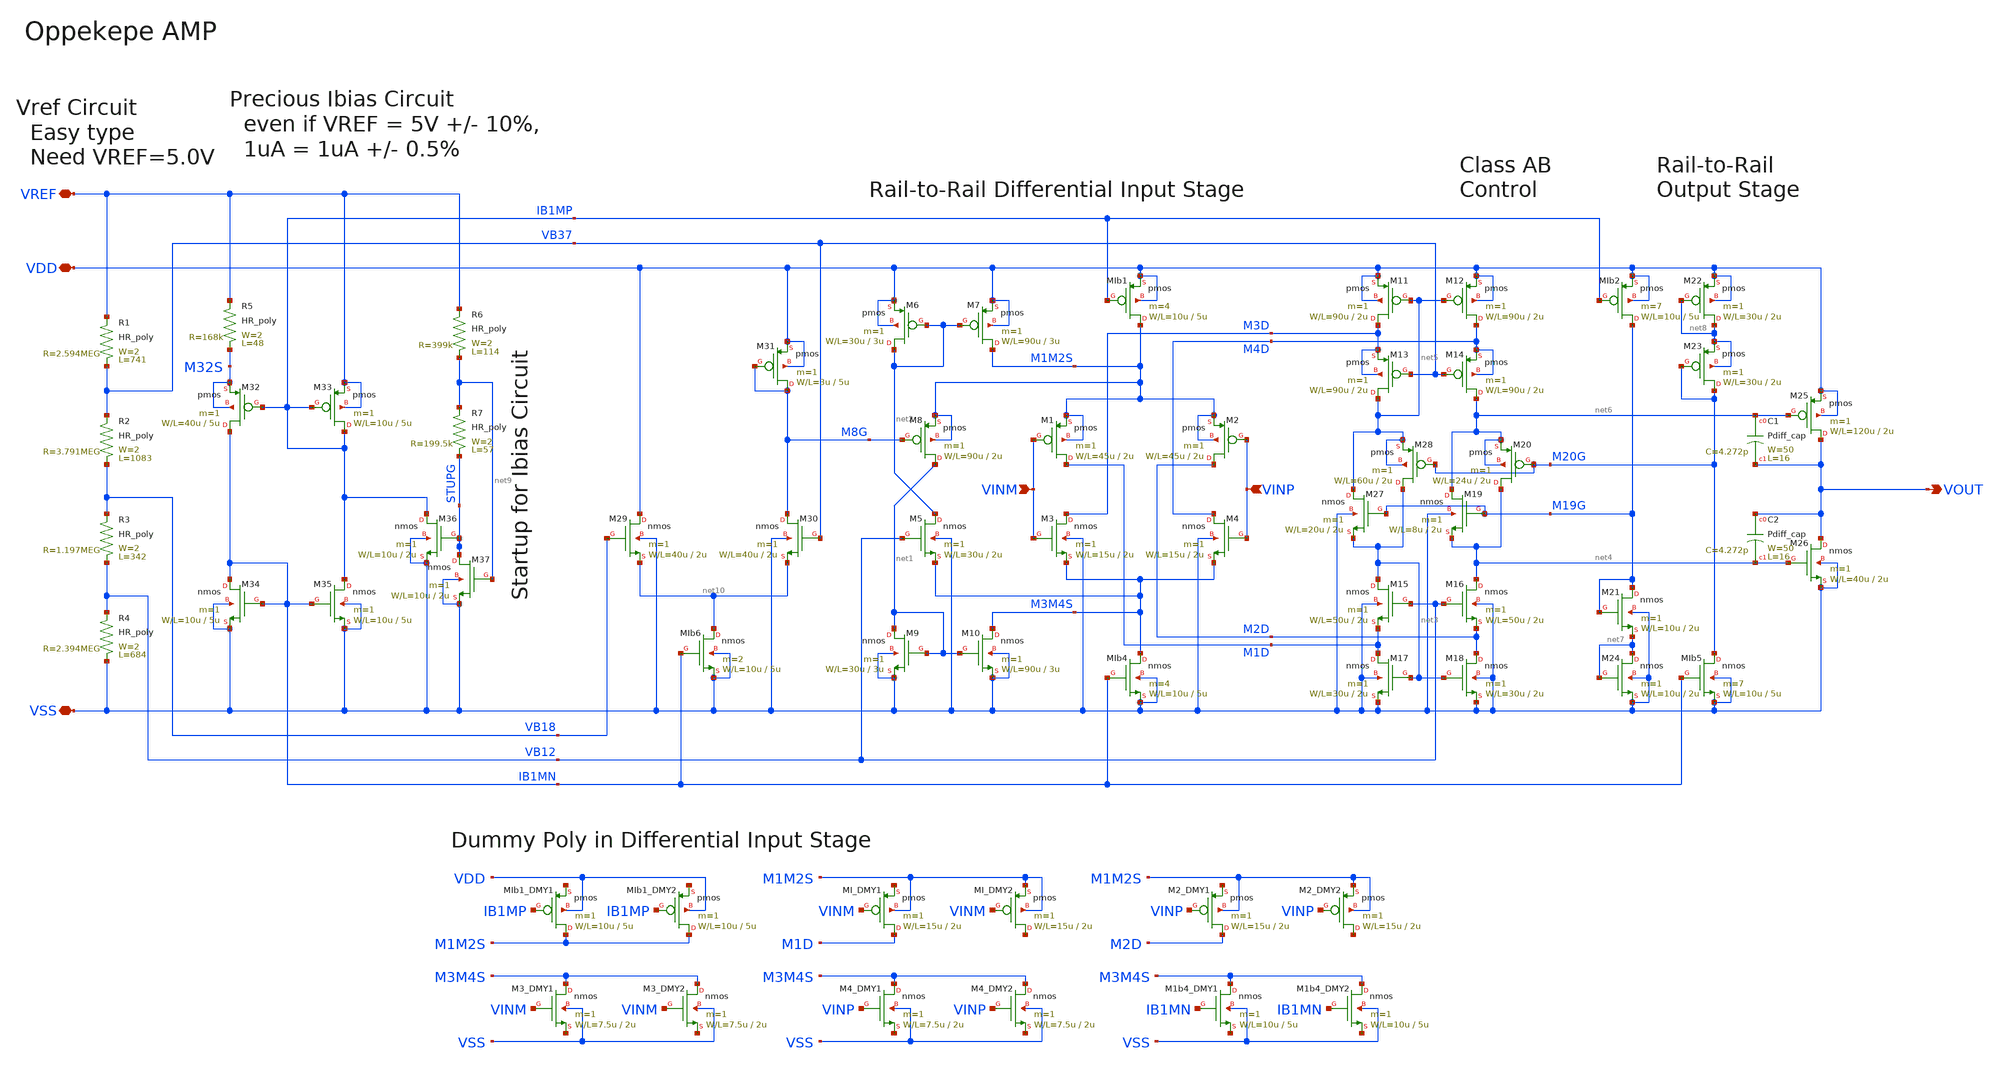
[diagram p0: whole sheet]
** sch_path: member_project/sanken/yamazaki/OppekepeAMP/OppekepeAMP.sch
**.subckt OppekepeAMP VDD VSS VINM VINP VOUT VREF
*.iopin VDD
*.iopin VSS
*.ipin VINM
*.ipin VINP
*.opin VOUT
*.iopin VREF
M29 VDD VB18 net10 VSS nmos L=2u W=40u m=1
M30 M8G VB37 net10 VSS nmos L=2u W=40u m=1
M31 M8G M8G VDD VDD pmos L=5u W=3u m=1
M10 M3M4S net1 VSS VSS nmos L=3u W=90u m=1
M9 net1 net1 VSS VSS nmos L=3u W=30u m=1
M8 net1 M8G M1M2S M1M2S pmos L=2u W=90u m=1
M7 M1M2S net2 VDD VDD pmos L=3u W=90u m=1
M6 net2 net2 VDD VDD pmos L=3u W=30u m=1
M4 M4D VINP M3M4S VSS nmos L=2u W=15u m=1
M3 M3D VINM M3M4S VSS nmos L=2u W=15u m=1
M1 M1D VINM M1M2S M1M2S pmos L=2u W=45u m=1
M2 M2D VINP M1M2S M1M2S pmos L=2u W=45u m=1
M5 net2 VB12 M3M4S VSS nmos L=2u W=30u m=1
M17 M1D net3 VSS VSS nmos L=2u W=30u m=1
M18 M2D net3 VSS VSS nmos L=2u W=30u m=1
M15 net3 VB12 M1D VSS nmos L=2u W=50u m=1
M16 net4 VB12 M2D VSS nmos L=2u W=50u m=1
M27 net5 M19G net3 VSS nmos L=2u W=20u m=1
M19 net6 M19G net4 VSS nmos L=2u W=8u m=1
M28 net3 M20G net5 net5 pmos L=2u W=60u m=1
M20 net4 M20G net6 net6 pmos L=2u W=24u m=1
M13 net5 VB37 M3D M3D pmos L=2u W=90u m=1
M14 net6 VB37 M4D M4D pmos L=2u W=90u m=1
M11 M3D net5 VDD VDD pmos L=2u W=90u m=1
M12 M4D net5 VDD VDD pmos L=2u W=90u m=1
M24 net7 net7 VSS VSS nmos L=2u W=10u m=1
M21 M19G M19G net7 VSS nmos L=2u W=10u m=1
M22 net8 net8 VDD VDD pmos L=2u W=30u m=1
M23 M20G M20G net8 net8 pmos L=2u W=30u m=1
M25 VOUT net6 VDD VDD pmos L=2u W=120u m=1
M26 VOUT net4 VSS VSS nmos L=2u W=40u m=1
M32 IB1MN IB1MP M32S M32S pmos L=5u W=40u m=1
M33 IB1MP IB1MP VREF VREF pmos L=5u W=10u m=1
M34 IB1MN IB1MN VSS VSS nmos L=5u W=10u m=1
M35 IB1MP IB1MN VSS VSS nmos L=5u W=10u m=1
M36 IB1MP STUPG VSS VSS nmos L=2u W=10u m=1
M37 STUPG net9 VSS VSS nmos L=2u W=10u m=1
MIb1 M1M2S IB1MP VDD VDD pmos L=5u W=10u m=4
MIb6 net10 IB1MN VSS VSS nmos L=5u W=10u m=2
MIb4 M3M4S IB1MN VSS VSS nmos L=5u W=10u m=4
MIb5 M20G IB1MN VSS VSS nmos L=5u W=10u m=7
MIb2 M19G IB1MP VDD VDD pmos L=5u W=10u m=7
C1 net6 VOUT Pdiff_cap W=50 L=16
C2 VOUT net4 Pdiff_cap W=50 L=16
MIb1_DMY1 M1M2S IB1MP net11 VDD pmos L=5u W=10u m=1
MIb1_DMY2 M1M2S IB1MP net12 VDD pmos L=5u W=10u m=1
MI_DMY1 M1D VINM net13 M1M2S pmos L=2u W=15u m=1
MI_DMY2 net14 VINM M1M2S M1M2S pmos L=2u W=15u m=1
M2_DMY1 M2D VINP net15 M1M2S pmos L=2u W=15u m=1
M2_DMY2 net16 VINP M1M2S M1M2S pmos L=2u W=15u m=1
M1b4_DMY1 M3M4S IB1MN net17 VSS nmos L=5u W=10u m=1
M1b4_DMY2 M3M4S IB1MN net18 VSS nmos L=5u W=10u m=1
R1 VB37 VREF HR_poly W=2 L=741
R2 VB18 VB37 HR_poly W=2 L=1083
R3 VB12 VB18 HR_poly W=2 L=342
R4 VSS VB12 HR_poly W=2 L=684
R5 M32S VREF HR_poly W=2 L=48
R6 net9 VREF HR_poly W=2 L=114
R7 STUPG net9 HR_poly W=2 L=57
M4_DMY1 M3M4S VINP net19 VSS nmos L=2u W=7.5u m=1
M4_DMY2 M3M4S VINP net20 VSS nmos L=2u W=7.5u m=1
M3_DMY1 M3M4S VINM net21 VSS nmos L=2u W=7.5u m=1
M3_DMY2 M3M4S VINM net22 VSS nmos L=2u W=7.5u m=1
**.ends
.end
